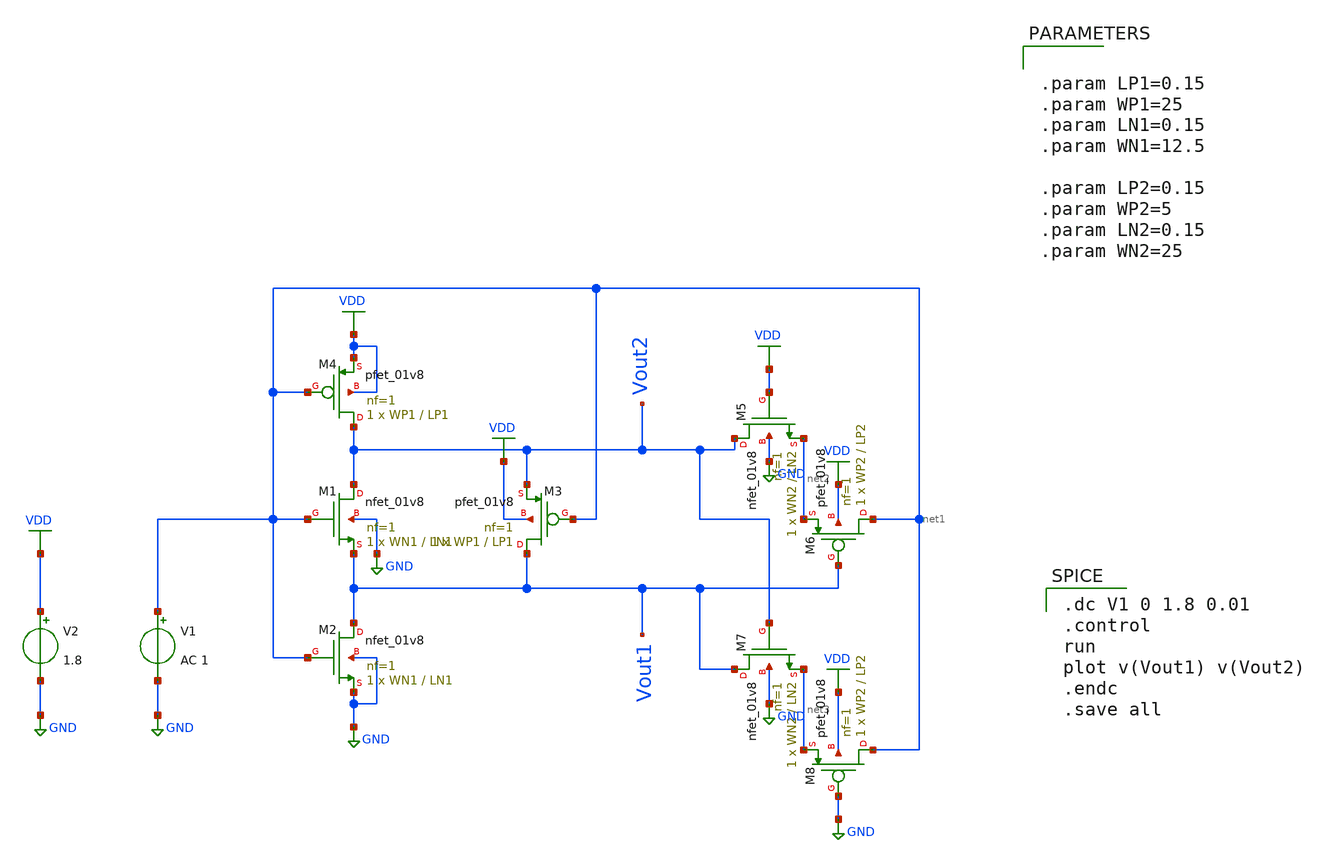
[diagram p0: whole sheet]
** sch_path: LIQAF circuit/Single Stage/single stage LIQAF.sch
**.subckt single stage LIQAF
XM1 Vout2 net1 Vout1 GND sky130_fd_pr__nfet_01v8 L=LN1 W=WN1 nf=1 ad='int((nf+1)/2) * W/nf * 0.29' as='int((nf+2)/2) * W/nf * 0.29'
+ pd='2*int((nf+1)/2) * (W/nf + 0.29)' ps='2*int((nf+2)/2) * (W/nf + 0.29)' nrd='0.29 / W' nrs='0.29 / W'
+ sa=0 sb=0 sd=0 mult=1 m=1
V1 net1 GND AC 1
V2 VDD GND 1.8
XM2 Vout1 net1 GND GND sky130_fd_pr__nfet_01v8 L=LN1 W=WN1 nf=1 ad='int((nf+1)/2) * W/nf * 0.29' as='int((nf+2)/2) * W/nf * 0.29'
+ pd='2*int((nf+1)/2) * (W/nf + 0.29)' ps='2*int((nf+2)/2) * (W/nf + 0.29)' nrd='0.29 / W' nrs='0.29 / W'
+ sa=0 sb=0 sd=0 mult=1 m=1
XM3 Vout1 net1 Vout2 VDD sky130_fd_pr__pfet_01v8 L=LP1 W=WP1 nf=1 ad='int((nf+1)/2) * W/nf * 0.29' as='int((nf+2)/2) * W/nf * 0.29'
+ pd='2*int((nf+1)/2) * (W/nf + 0.29)' ps='2*int((nf+2)/2) * (W/nf + 0.29)' nrd='0.29 / W' nrs='0.29 / W'
+ sa=0 sb=0 sd=0 mult=1 m=1
XM4 Vout2 net1 VDD VDD sky130_fd_pr__pfet_01v8 L=LP1 W=WP1 nf=1 ad='int((nf+1)/2) * W/nf * 0.29' as='int((nf+2)/2) * W/nf * 0.29'
+ pd='2*int((nf+1)/2) * (W/nf + 0.29)' ps='2*int((nf+2)/2) * (W/nf + 0.29)' nrd='0.29 / W' nrs='0.29 / W'
+ sa=0 sb=0 sd=0 mult=1 m=1
XM5 Vout2 VDD net2 GND sky130_fd_pr__nfet_01v8 L=LN2 W=WN2 nf=1 ad='int((nf+1)/2) * W/nf * 0.29' as='int((nf+2)/2) * W/nf * 0.29'
+ pd='2*int((nf+1)/2) * (W/nf + 0.29)' ps='2*int((nf+2)/2) * (W/nf + 0.29)' nrd='0.29 / W' nrs='0.29 / W'
+ sa=0 sb=0 sd=0 mult=1 m=1
XM6 net1 Vout1 net2 VDD sky130_fd_pr__pfet_01v8 L=LP2 W=WP2 nf=1 ad='int((nf+1)/2) * W/nf * 0.29' as='int((nf+2)/2) * W/nf * 0.29'
+ pd='2*int((nf+1)/2) * (W/nf + 0.29)' ps='2*int((nf+2)/2) * (W/nf + 0.29)' nrd='0.29 / W' nrs='0.29 / W'
+ sa=0 sb=0 sd=0 mult=1 m=1
XM7 Vout1 Vout2 net3 GND sky130_fd_pr__nfet_01v8 L=LN2 W=WN2 nf=1 ad='int((nf+1)/2) * W/nf * 0.29' as='int((nf+2)/2) * W/nf * 0.29'
+ pd='2*int((nf+1)/2) * (W/nf + 0.29)' ps='2*int((nf+2)/2) * (W/nf + 0.29)' nrd='0.29 / W' nrs='0.29 / W'
+ sa=0 sb=0 sd=0 mult=1 m=1
XM8 net1 GND net3 VDD sky130_fd_pr__pfet_01v8 L=LP2 W=WP2 nf=1 ad='int((nf+1)/2) * W/nf * 0.29' as='int((nf+2)/2) * W/nf * 0.29'
+ pd='2*int((nf+1)/2) * (W/nf + 0.29)' ps='2*int((nf+2)/2) * (W/nf + 0.29)' nrd='0.29 / W' nrs='0.29 / W'
+ sa=0 sb=0 sd=0 mult=1 m=1
**** begin user architecture code
 ** manual skywater pdks install (with patches applied)
* .lib $::SKYWATER_MODELS/models/sky130.lib.spice tt

** opencircuitdesign pdks install
.lib $::SKYWATER_MODELS/sky130.lib.spice tt

.param mc_mm_switch=0
.param mc_pr_switch=0


.dc V1 0 1.8 0.01
.control
run
plot v(Vout1) v(Vout2)
.endc
.save all



.param LP1=0.15
.param WP1=25
.param LN1=0.15
.param WN1=12.5

.param LP2=0.15
.param WP2=5
.param LN2=0.15
.param WN2=25


**** end user architecture code
**.ends
.GLOBAL GND
.GLOBAL VDD
.end
